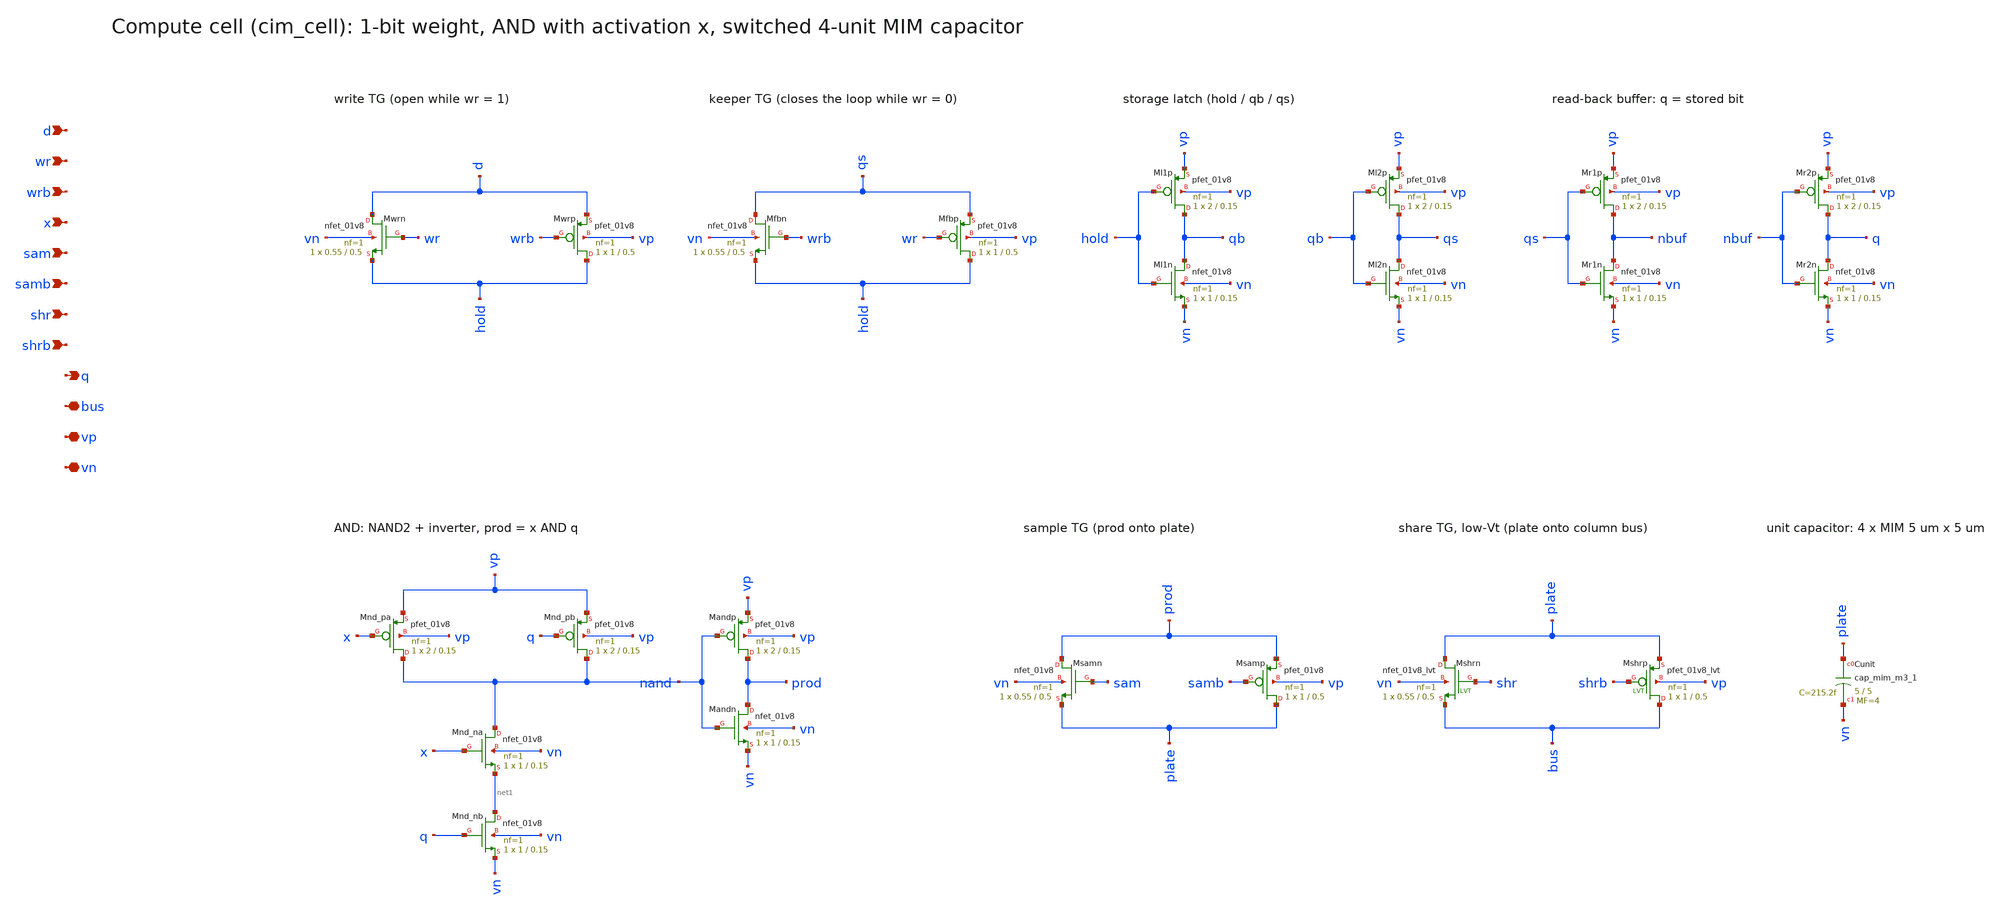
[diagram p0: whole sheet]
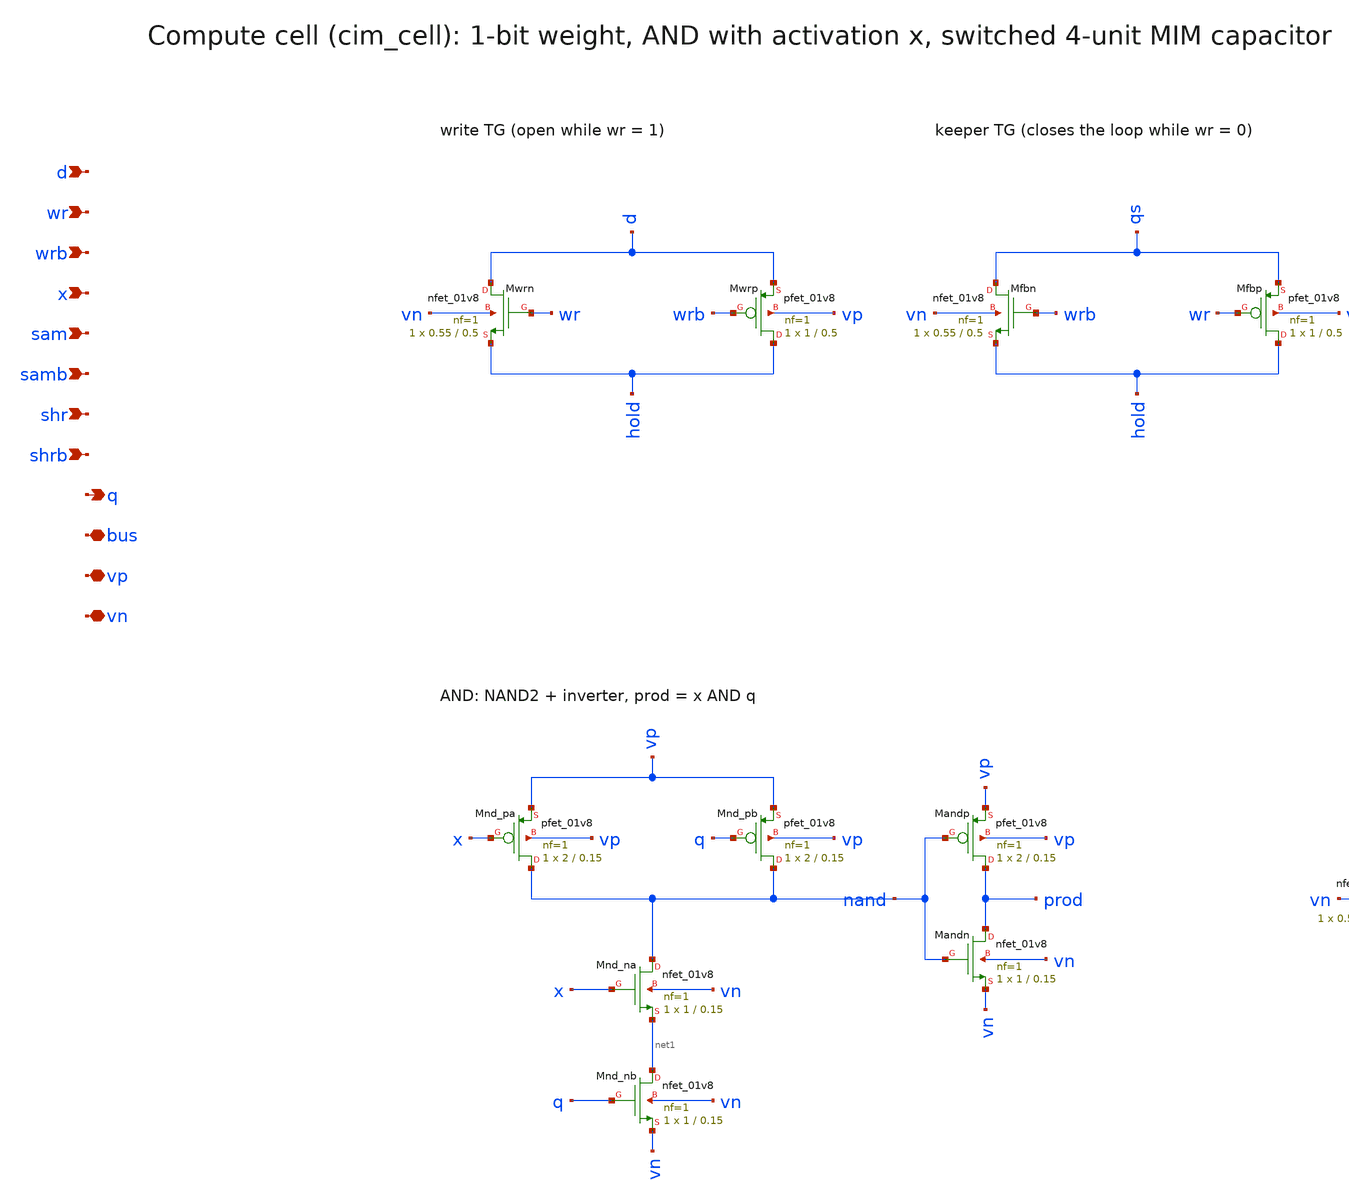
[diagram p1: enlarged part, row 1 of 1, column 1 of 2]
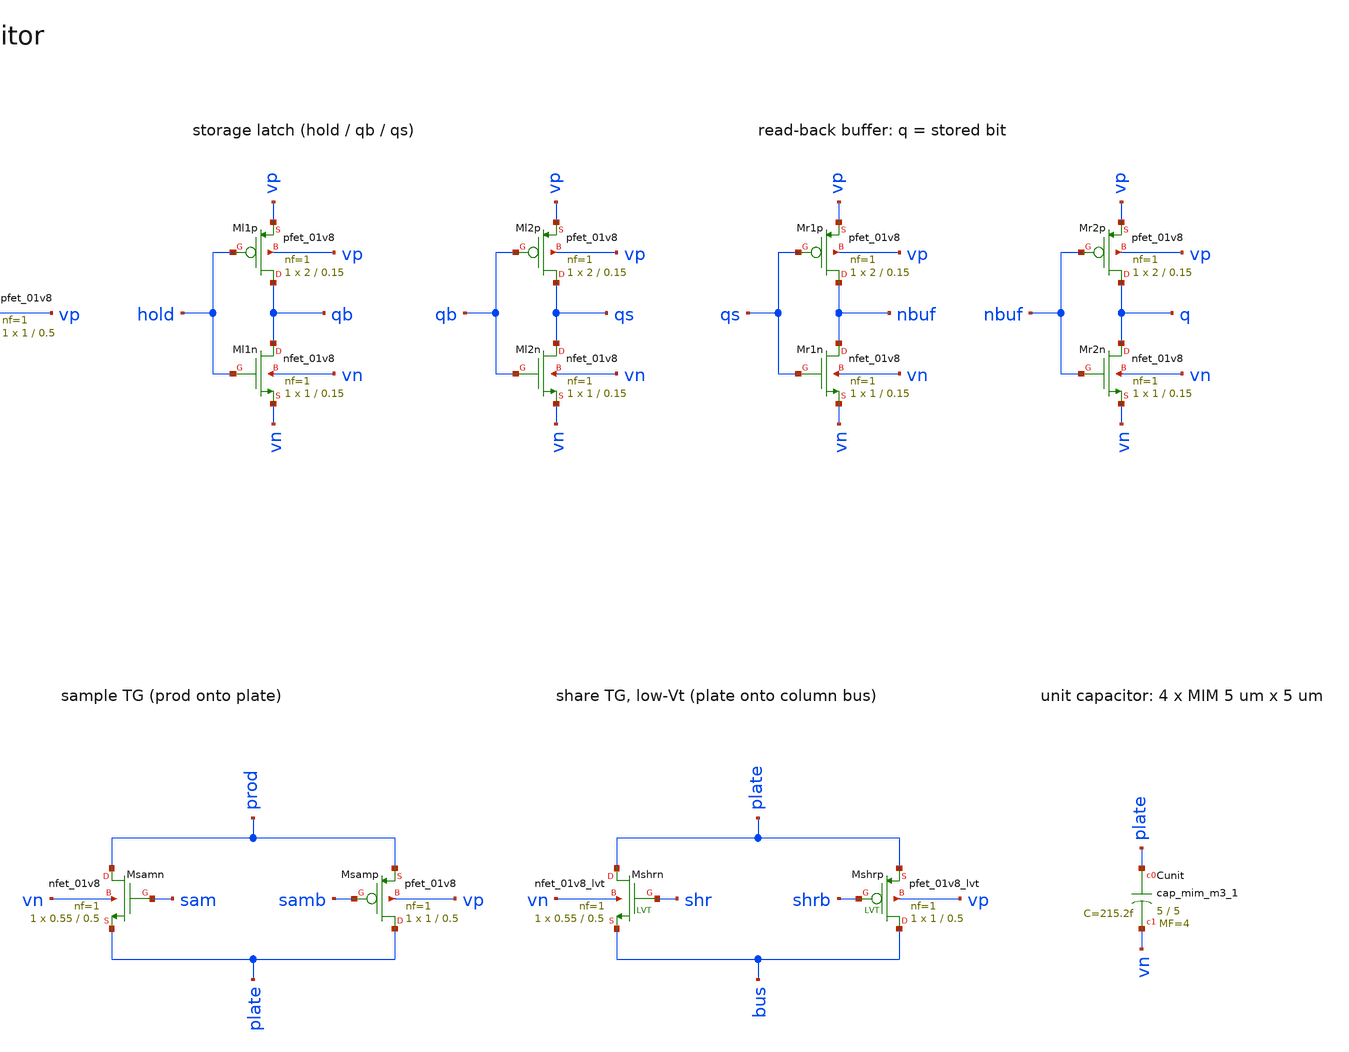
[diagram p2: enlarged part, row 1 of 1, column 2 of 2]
** sch_path: xschem/cim_cell.sch
**.subckt cim_cell d wr wrb x sam samb shr shrb q bus vp vn
*.ipin d
*.ipin wr
*.ipin wrb
*.ipin x
*.ipin sam
*.ipin samb
*.ipin shr
*.ipin shrb
*.opin q
*.iopin bus
*.iopin vp
*.iopin vn
XMwrn d wr hold vn sky130_fd_pr__nfet_01v8 L=0.5 W=0.55 nf=1 ad='int((nf+1)/2) * W/nf * 0.29' as='int((nf+2)/2) * W/nf * 0.29'
+ pd='2*int((nf+1)/2) * (W/nf + 0.29)' ps='2*int((nf+2)/2) * (W/nf + 0.29)' nrd=0 nrs=0 sa=0 sb=0 sd=0
+ mult=1 m=1
XMwrp hold wrb d vp sky130_fd_pr__pfet_01v8 L=0.5 W=1 nf=1 ad='int((nf+1)/2) * W/nf * 0.29' as='int((nf+2)/2) * W/nf * 0.29'
+ pd='2*int((nf+1)/2) * (W/nf + 0.29)' ps='2*int((nf+2)/2) * (W/nf + 0.29)' nrd=0 nrs=0 sa=0 sb=0 sd=0
+ mult=1 m=1
XMfbn qs wrb hold vn sky130_fd_pr__nfet_01v8 L=0.5 W=0.55 nf=1 ad='int((nf+1)/2) * W/nf * 0.29' as='int((nf+2)/2) * W/nf * 0.29'
+ pd='2*int((nf+1)/2) * (W/nf + 0.29)' ps='2*int((nf+2)/2) * (W/nf + 0.29)' nrd=0 nrs=0 sa=0 sb=0 sd=0
+ mult=1 m=1
XMfbp hold wr qs vp sky130_fd_pr__pfet_01v8 L=0.5 W=1 nf=1 ad='int((nf+1)/2) * W/nf * 0.29' as='int((nf+2)/2) * W/nf * 0.29'
+ pd='2*int((nf+1)/2) * (W/nf + 0.29)' ps='2*int((nf+2)/2) * (W/nf + 0.29)' nrd=0 nrs=0 sa=0 sb=0 sd=0
+ mult=1 m=1
XMl1p qb hold vp vp sky130_fd_pr__pfet_01v8 L=0.15 W=2 nf=1 ad='int((nf+1)/2) * W/nf * 0.29' as='int((nf+2)/2) * W/nf * 0.29'
+ pd='2*int((nf+1)/2) * (W/nf + 0.29)' ps='2*int((nf+2)/2) * (W/nf + 0.29)' nrd=0 nrs=0 sa=0 sb=0 sd=0
+ mult=1 m=1
XMl1n qb hold vn vn sky130_fd_pr__nfet_01v8 L=0.15 W=1 nf=1 ad='int((nf+1)/2) * W/nf * 0.29' as='int((nf+2)/2) * W/nf * 0.29'
+ pd='2*int((nf+1)/2) * (W/nf + 0.29)' ps='2*int((nf+2)/2) * (W/nf + 0.29)' nrd=0 nrs=0 sa=0 sb=0 sd=0
+ mult=1 m=1
XMl2p qs qb vp vp sky130_fd_pr__pfet_01v8 L=0.15 W=2 nf=1 ad='int((nf+1)/2) * W/nf * 0.29' as='int((nf+2)/2) * W/nf * 0.29'
+ pd='2*int((nf+1)/2) * (W/nf + 0.29)' ps='2*int((nf+2)/2) * (W/nf + 0.29)' nrd=0 nrs=0 sa=0 sb=0 sd=0
+ mult=1 m=1
XMl2n qs qb vn vn sky130_fd_pr__nfet_01v8 L=0.15 W=1 nf=1 ad='int((nf+1)/2) * W/nf * 0.29' as='int((nf+2)/2) * W/nf * 0.29'
+ pd='2*int((nf+1)/2) * (W/nf + 0.29)' ps='2*int((nf+2)/2) * (W/nf + 0.29)' nrd=0 nrs=0 sa=0 sb=0 sd=0
+ mult=1 m=1
XMr1p nbuf qs vp vp sky130_fd_pr__pfet_01v8 L=0.15 W=2 nf=1 ad='int((nf+1)/2) * W/nf * 0.29' as='int((nf+2)/2) * W/nf * 0.29'
+ pd='2*int((nf+1)/2) * (W/nf + 0.29)' ps='2*int((nf+2)/2) * (W/nf + 0.29)' nrd=0 nrs=0 sa=0 sb=0 sd=0
+ mult=1 m=1
XMr1n nbuf qs vn vn sky130_fd_pr__nfet_01v8 L=0.15 W=1 nf=1 ad='int((nf+1)/2) * W/nf * 0.29' as='int((nf+2)/2) * W/nf * 0.29'
+ pd='2*int((nf+1)/2) * (W/nf + 0.29)' ps='2*int((nf+2)/2) * (W/nf + 0.29)' nrd=0 nrs=0 sa=0 sb=0 sd=0
+ mult=1 m=1
XMr2p q nbuf vp vp sky130_fd_pr__pfet_01v8 L=0.15 W=2 nf=1 ad='int((nf+1)/2) * W/nf * 0.29' as='int((nf+2)/2) * W/nf * 0.29'
+ pd='2*int((nf+1)/2) * (W/nf + 0.29)' ps='2*int((nf+2)/2) * (W/nf + 0.29)' nrd=0 nrs=0 sa=0 sb=0 sd=0
+ mult=1 m=1
XMr2n q nbuf vn vn sky130_fd_pr__nfet_01v8 L=0.15 W=1 nf=1 ad='int((nf+1)/2) * W/nf * 0.29' as='int((nf+2)/2) * W/nf * 0.29'
+ pd='2*int((nf+1)/2) * (W/nf + 0.29)' ps='2*int((nf+2)/2) * (W/nf + 0.29)' nrd=0 nrs=0 sa=0 sb=0 sd=0
+ mult=1 m=1
XMnd_pa nand x vp vp sky130_fd_pr__pfet_01v8 L=0.15 W=2 nf=1 ad='int((nf+1)/2) * W/nf * 0.29' as='int((nf+2)/2) * W/nf * 0.29'
+ pd='2*int((nf+1)/2) * (W/nf + 0.29)' ps='2*int((nf+2)/2) * (W/nf + 0.29)' nrd=0 nrs=0 sa=0 sb=0 sd=0
+ mult=1 m=1
XMnd_pb nand q vp vp sky130_fd_pr__pfet_01v8 L=0.15 W=2 nf=1 ad='int((nf+1)/2) * W/nf * 0.29' as='int((nf+2)/2) * W/nf * 0.29'
+ pd='2*int((nf+1)/2) * (W/nf + 0.29)' ps='2*int((nf+2)/2) * (W/nf + 0.29)' nrd=0 nrs=0 sa=0 sb=0 sd=0
+ mult=1 m=1
XMnd_na nand x net1 vn sky130_fd_pr__nfet_01v8 L=0.15 W=1 nf=1 ad='int((nf+1)/2) * W/nf * 0.29' as='int((nf+2)/2) * W/nf * 0.29'
+ pd='2*int((nf+1)/2) * (W/nf + 0.29)' ps='2*int((nf+2)/2) * (W/nf + 0.29)' nrd=0 nrs=0 sa=0 sb=0 sd=0
+ mult=1 m=1
XMnd_nb net1 q vn vn sky130_fd_pr__nfet_01v8 L=0.15 W=1 nf=1 ad='int((nf+1)/2) * W/nf * 0.29' as='int((nf+2)/2) * W/nf * 0.29'
+ pd='2*int((nf+1)/2) * (W/nf + 0.29)' ps='2*int((nf+2)/2) * (W/nf + 0.29)' nrd=0 nrs=0 sa=0 sb=0 sd=0
+ mult=1 m=1
XMandp prod nand vp vp sky130_fd_pr__pfet_01v8 L=0.15 W=2 nf=1 ad='int((nf+1)/2) * W/nf * 0.29' as='int((nf+2)/2) * W/nf * 0.29'
+ pd='2*int((nf+1)/2) * (W/nf + 0.29)' ps='2*int((nf+2)/2) * (W/nf + 0.29)' nrd=0 nrs=0 sa=0 sb=0 sd=0
+ mult=1 m=1
XMandn prod nand vn vn sky130_fd_pr__nfet_01v8 L=0.15 W=1 nf=1 ad='int((nf+1)/2) * W/nf * 0.29' as='int((nf+2)/2) * W/nf * 0.29'
+ pd='2*int((nf+1)/2) * (W/nf + 0.29)' ps='2*int((nf+2)/2) * (W/nf + 0.29)' nrd=0 nrs=0 sa=0 sb=0 sd=0
+ mult=1 m=1
XMsamn prod sam plate vn sky130_fd_pr__nfet_01v8 L=0.5 W=0.55 nf=1 ad='int((nf+1)/2) * W/nf * 0.29' as='int((nf+2)/2) * W/nf * 0.29'
+ pd='2*int((nf+1)/2) * (W/nf + 0.29)' ps='2*int((nf+2)/2) * (W/nf + 0.29)' nrd=0 nrs=0 sa=0 sb=0 sd=0
+ mult=1 m=1
XMsamp plate samb prod vp sky130_fd_pr__pfet_01v8 L=0.5 W=1 nf=1 ad='int((nf+1)/2) * W/nf * 0.29' as='int((nf+2)/2) * W/nf * 0.29'
+ pd='2*int((nf+1)/2) * (W/nf + 0.29)' ps='2*int((nf+2)/2) * (W/nf + 0.29)' nrd=0 nrs=0 sa=0 sb=0 sd=0
+ mult=1 m=1
XMshrn plate shr bus vn sky130_fd_pr__nfet_01v8_lvt L=0.5 W=0.55 nf=1 ad='int((nf+1)/2) * W/nf * 0.29'
+ as='int((nf+2)/2) * W/nf * 0.29' pd='2*int((nf+1)/2) * (W/nf + 0.29)' ps='2*int((nf+2)/2) * (W/nf + 0.29)'
+ nrd=0 nrs=0 sa=0 sb=0 sd=0 mult=1 m=1
XMshrp bus shrb plate vp sky130_fd_pr__pfet_01v8_lvt L=0.5 W=1 nf=1 ad='int((nf+1)/2) * W/nf * 0.29'
+ as='int((nf+2)/2) * W/nf * 0.29' pd='2*int((nf+1)/2) * (W/nf + 0.29)' ps='2*int((nf+2)/2) * (W/nf + 0.29)'
+ nrd=0 nrs=0 sa=0 sb=0 sd=0 mult=1 m=1
XCunit plate vn sky130_fd_pr__cap_mim_m3_1 W=5 L=5 MF=4 m=4
**.ends
.end
